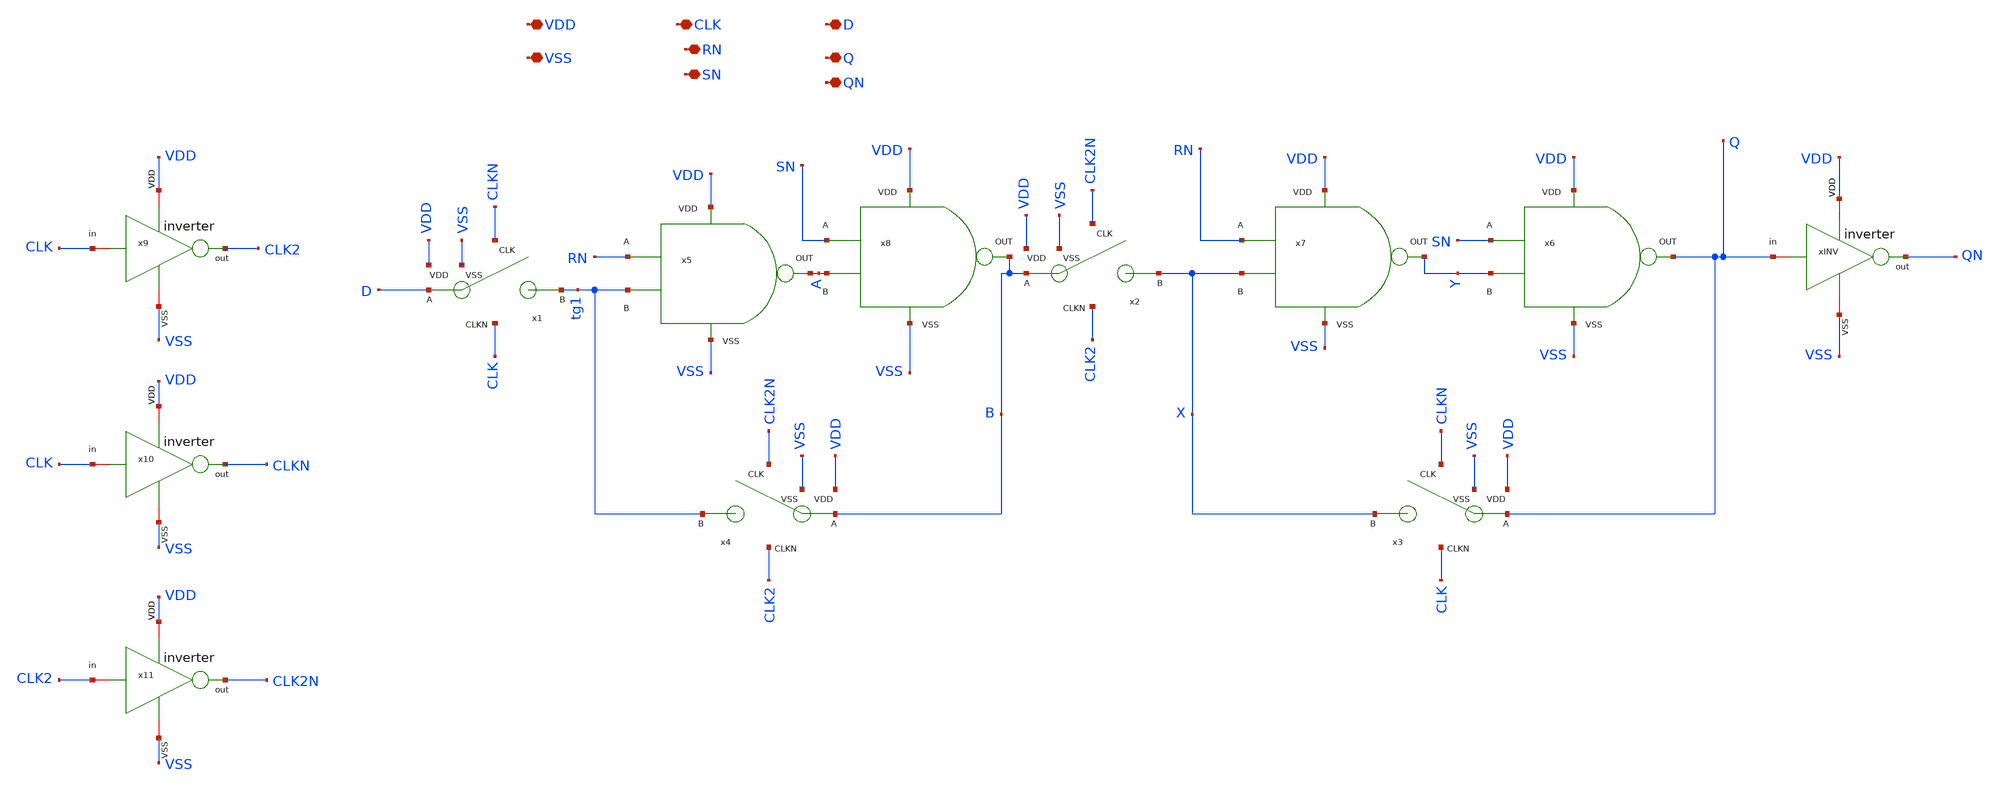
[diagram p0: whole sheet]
** sch_path: designs/sar_adc/digital/flip_flop_set/xschem/flip_flop_set.sch
**.subckt flip_flop_set VDD VSS CLK D RN Q QN SN
*.iopin VDD
*.iopin VSS
*.iopin CLK
*.iopin D
*.iopin RN
*.iopin Q
*.iopin QN
*.iopin SN
x1 CLKN D VDD tg1 CLK VSS TG
x2 CLK2N B VDD X CLK2 VSS TG
x3 CLKN Q VDD X CLK VSS TG
x4 CLK2N B VDD tg1 CLK2 VSS TG
x5 VDD VSS RN tg1 A NAND
x6 VDD VSS SN Y Q NAND
x9 VDD CLK CLK2 VSS inverter
x10 VDD CLK CLKN VSS inverter
x11 VDD CLK2 CLK2N VSS inverter
xINV VDD Q QN VSS inverter
x8 VDD VSS SN A B NAND
x7 VDD VSS RN X Y NAND
**.ends

* expanding   symbol:  designs/sar_adc/digital/TG/xschem/TG.sym # of pins=6
** sym_path: designs/sar_adc/digital/TG/xschem/TG.sym
** sch_path: designs/sar_adc/digital/TG/xschem/TG.sch
.subckt TG CLK A VDD B CLKN VSS
*.iopin VDD
*.iopin VSS
*.ipin CLK
*.ipin CLKN
*.iopin A
*.iopin B
XM1 A CLK B VSS nfet_03v3 L=0.28u W=0.22u nf=1 ad='int((nf+1)/2) * W/nf * 0.18u' as='int((nf+2)/2) * W/nf * 0.18u'
+ pd='2*int((nf+1)/2) * (W/nf + 0.18u)' ps='2*int((nf+2)/2) * (W/nf + 0.18u)' nrd='0.18u / W' nrs='0.18u / W'
+ sa=0 sb=0 sd=0 m=1
XM2 A CLKN B VDD pfet_03v3 L=0.28u W=0.22u nf=1 ad='int((nf+1)/2) * W/nf * 0.18u' as='int((nf+2)/2) * W/nf * 0.18u'
+ pd='2*int((nf+1)/2) * (W/nf + 0.18u)' ps='2*int((nf+2)/2) * (W/nf + 0.18u)' nrd='0.18u / W' nrs='0.18u / W'
+ sa=0 sb=0 sd=0 m=1
.ends


* expanding   symbol:  designs/sar_adc/digital/NAND/xschem/NAND.sym # of pins=5
** sym_path: designs/sar_adc/digital/NAND/xschem/NAND.sym
** sch_path: designs/sar_adc/digital/NAND/xschem/NAND.sch
.subckt NAND VDD VSS A B out
*.iopin VDD
*.iopin A
*.iopin B
*.iopin out
*.iopin VSS
xINVA VDD net1 net2 VSS inverter
xINVB[2] VDD net2 out VSS inverter
xINVB[1] VDD net2 out VSS inverter
xINVB[0] VDD net2 out VSS inverter
XM2 net1 A VDD VDD pfet_03v3 L=0.28u W=0.5u nf=1 ad='int((nf+1)/2) * W/nf * 0.18u' as='int((nf+2)/2) * W/nf * 0.18u'
+ pd='2*int((nf+1)/2) * (W/nf + 0.18u)' ps='2*int((nf+2)/2) * (W/nf + 0.18u)' nrd='0.18u / W' nrs='0.18u / W'
+ sa=0 sb=0 sd=0 m=2
XM1 net1 A net3 VSS nfet_03v3 L=0.28u W=0.5u nf=1 ad='int((nf+1)/2) * W/nf * 0.18u' as='int((nf+2)/2) * W/nf * 0.18u'
+ pd='2*int((nf+1)/2) * (W/nf + 0.18u)' ps='2*int((nf+2)/2) * (W/nf + 0.18u)' nrd='0.18u / W' nrs='0.18u / W'
+ sa=0 sb=0 sd=0 m=1
XM3 net1 B VDD VDD pfet_03v3 L=0.28u W=0.5u nf=1 ad='int((nf+1)/2) * W/nf * 0.18u' as='int((nf+2)/2) * W/nf * 0.18u'
+ pd='2*int((nf+1)/2) * (W/nf + 0.18u)' ps='2*int((nf+2)/2) * (W/nf + 0.18u)' nrd='0.18u / W' nrs='0.18u / W'
+ sa=0 sb=0 sd=0 m=2
XM4 net3 B VSS VSS nfet_03v3 L=0.28u W=0.5u nf=1 ad='int((nf+1)/2) * W/nf * 0.18u' as='int((nf+2)/2) * W/nf * 0.18u'
+ pd='2*int((nf+1)/2) * (W/nf + 0.18u)' ps='2*int((nf+2)/2) * (W/nf + 0.18u)' nrd='0.18u / W' nrs='0.18u / W'
+ sa=0 sb=0 sd=0 m=1
.ends


* expanding   symbol:  designs/sar_adc/digital/inverter/xschem/inverter.sym # of pins=6
** sym_path: designs/sar_adc/digital/inverter/xschem/inverter.sym
** sch_path: designs/sar_adc/digital/inverter/xschem/inverter.sch
.subckt inverter VDD in out VSS
*.opin out
*.iopin in
*.iopin VDD
*.iopin VSS
XM1 out in VSS VSS nfet_03v3 L=0.28u W=1u nf=1 ad='int((nf+1)/2) * W/nf * 0.18u' as='int((nf+2)/2) * W/nf * 0.18u'
+ pd='2*int((nf+1)/2) * (W/nf + 0.18u)' ps='2*int((nf+2)/2) * (W/nf + 0.18u)' nrd='0.18u / W' nrs='0.18u / W'
+ sa=0 sb=0 sd=0 m=1
XM2 out in VDD VDD pfet_03v3 L=0.28u W=3u nf=1 ad='int((nf+1)/2) * W/nf * 0.18u' as='int((nf+2)/2) * W/nf * 0.18u'
+ pd='2*int((nf+1)/2) * (W/nf + 0.18u)' ps='2*int((nf+2)/2) * (W/nf + 0.18u)' nrd='0.18u / W' nrs='0.18u / W'
+ sa=0 sb=0 sd=0 m=1
.ends

.end
